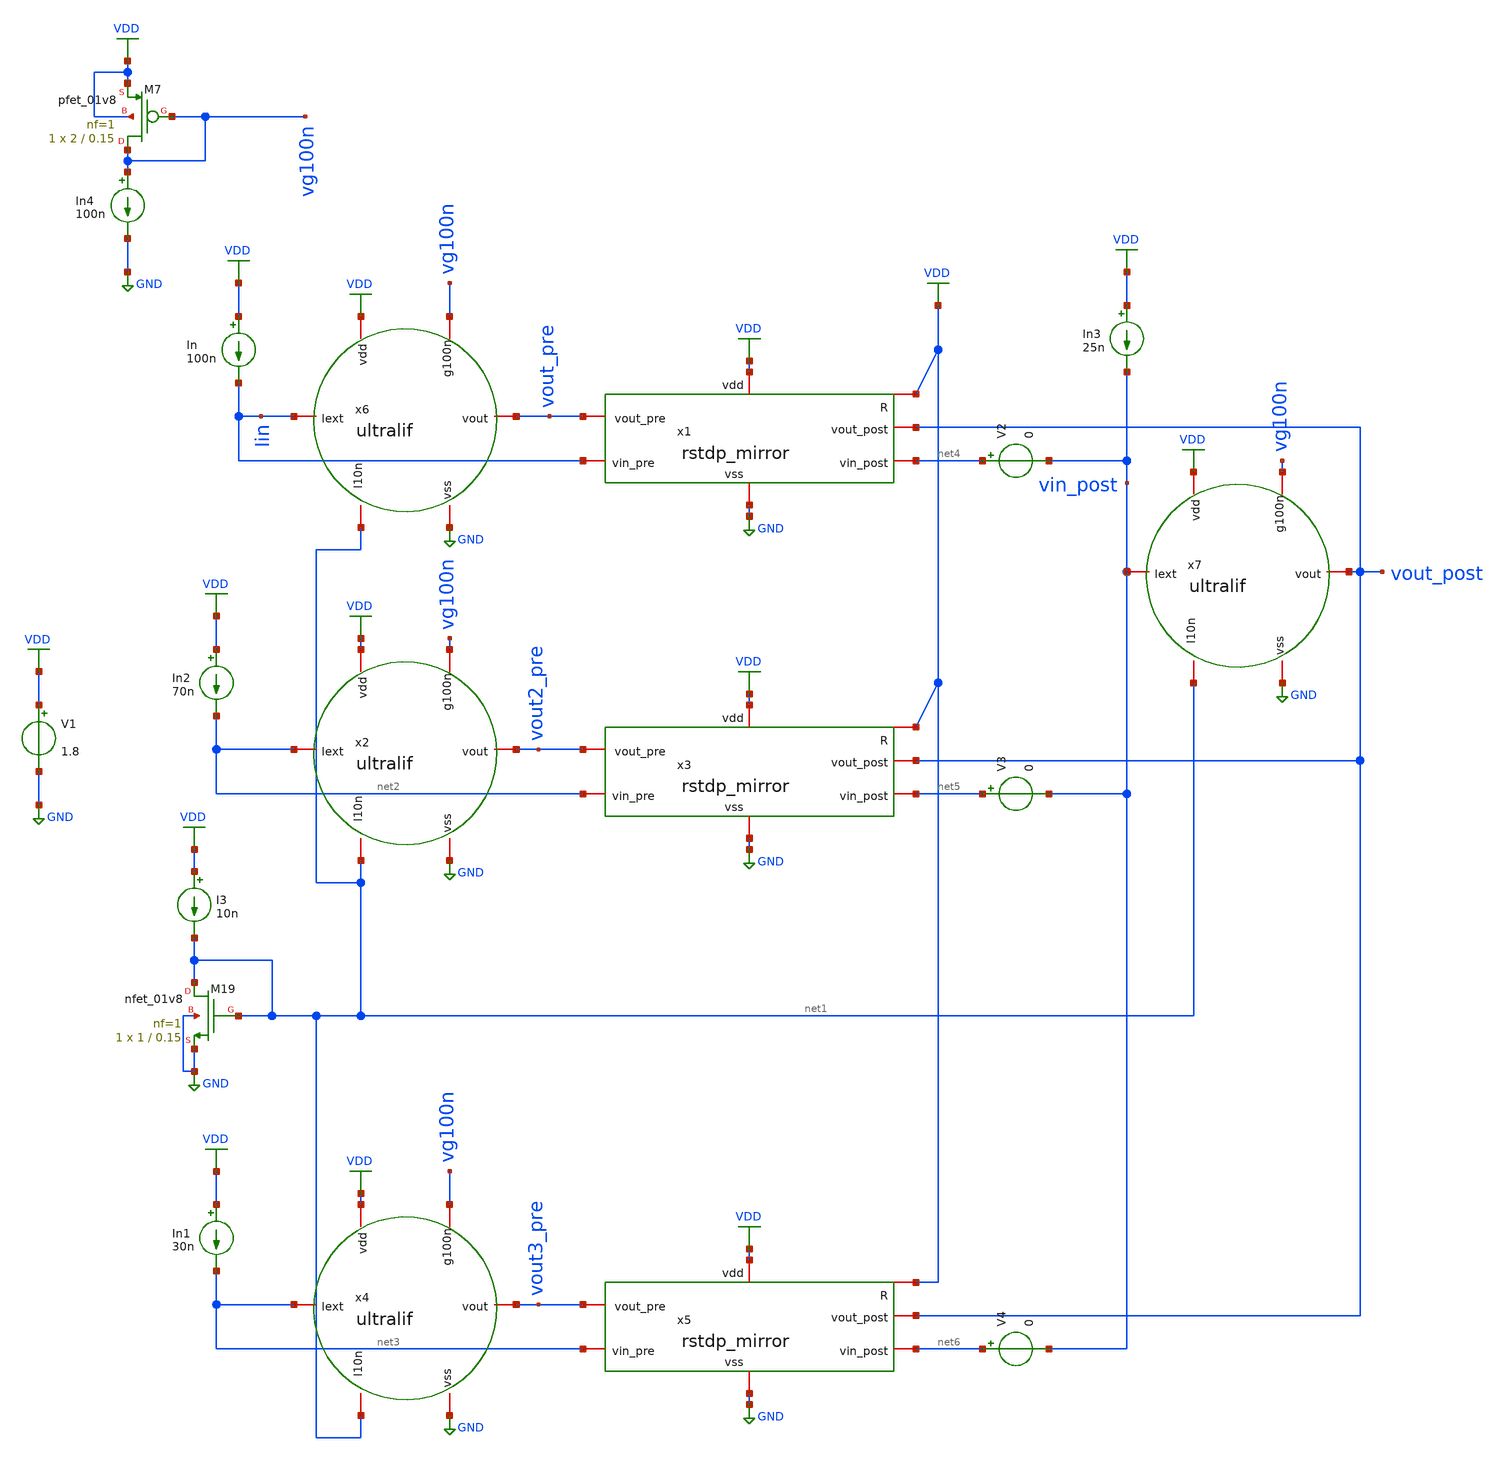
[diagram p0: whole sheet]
** sch_path: tb_3_1_mirror.sch
**.subckt tb_3_1_mirror
V1 VDD GND 1.8
x6 VDD Iin vout_pre net1 GND vg100n ultralif
x7 VDD vin_post vout_post net1 GND vg100n ultralif
XM19 net1 net1 GND GND sky130_fd_pr__nfet_01v8 L=0.15 W=1 nf=1 ad='int((nf+1)/2) * W/nf * 0.29' as='int((nf+2)/2) * W/nf * 0.29'
+ pd='2*int((nf+1)/2) * (W/nf + 0.29)' ps='2*int((nf+2)/2) * (W/nf + 0.29)' nrd='0.29 / W' nrs='0.29 / W'
+ sa=0 sb=0 sd=0 mult=1 m=1
I3 VDD net1 10n
In VDD Iin 100n
x2 VDD net2 vout2_pre net1 GND vg100n ultralif
In2 VDD net2 70n
x4 VDD net3 vout3_pre net1 GND vg100n ultralif
In1 VDD net3 30n
In3 VDD vin_post 25n
XM7 vg100n vg100n VDD VDD sky130_fd_pr__pfet_01v8 L=0.15 W=2 nf=1 ad='int((nf+1)/2) * W/nf * 0.29' as='int((nf+2)/2) * W/nf * 0.29'
+ pd='2*int((nf+1)/2) * (W/nf + 0.29)' ps='2*int((nf+2)/2) * (W/nf + 0.29)' nrd='0.29 / W' nrs='0.29 / W'
+ sa=0 sb=0 sd=0 mult=1 m=1
In4 vg100n GND 100n
x1 VDD VDD GND vout_pre vout_post net4 Iin rstdp_mirror
x3 VDD VDD GND vout2_pre vout_post net5 net2 rstdp_mirror
x5 VDD VDD GND vout3_pre vout_post net6 net3 rstdp_mirror
V2 net4 vin_post 0
V3 net5 vin_post 0
V4 net6 vin_post 0
**** begin user architecture code
.lib $::SKYWATER_MODELS/sky130.lib.spice tt

** opencircuitdesign pdks install
.inc $::SKYWATER_MODELS/rram_v0.spice

**** end user architecture code
**.ends

* expanding   symbol:  /home/alex/Desktop/EDA/SNN_IPN/Neuron/ultralif/ultralif.sym # of pins=6
** sym_path: Neuron/ultralif/ultralif.sym
** sch_path: Neuron/ultralif/ultralif.sch
.subckt ultralif vdd Iext vout I10n vss g100n
*.iopin Iext
*.iopin vout
*.iopin vss
*.iopin I10n
*.iopin vdd
*.iopin g100n
XM1 net2 net2 vm vdd sky130_fd_pr__pfet_01v8 L=10 W=1 nf=1 ad='int((nf+1)/2) * W/nf * 0.29' as='int((nf+2)/2) * W/nf * 0.29'
+ pd='2*int((nf+1)/2) * (W/nf + 0.29)' ps='2*int((nf+2)/2) * (W/nf + 0.29)' nrd='0.29 / W' nrs='0.29 / W'
+ sa=0 sb=0 sd=0 mult=1 m=1
XM2 net2 net1 vm vdd sky130_fd_pr__pfet_01v8 L=0.15 W=1.5 nf=1 ad='int((nf+1)/2) * W/nf * 0.29' as='int((nf+2)/2) * W/nf * 0.29'
+ pd='2*int((nf+1)/2) * (W/nf + 0.29)' ps='2*int((nf+2)/2) * (W/nf + 0.29)' nrd='0.29 / W' nrs='0.29 / W'
+ sa=0 sb=0 sd=0 mult=1 m=1
XM3 net1 net1 vm vdd sky130_fd_pr__pfet_01v8 L=0.15 W=5 nf=1 ad='int((nf+1)/2) * W/nf * 0.29' as='int((nf+2)/2) * W/nf * 0.29'
+ pd='2*int((nf+1)/2) * (W/nf + 0.29)' ps='2*int((nf+2)/2) * (W/nf + 0.29)' nrd='0.29 / W' nrs='0.29 / W'
+ sa=0 sb=0 sd=0 mult=2 m=2
XM4 net1 net2 vss vss sky130_fd_pr__nfet_01v8 L=4 W=1 nf=1 ad='int((1 + 1)/2) * 1 / 1 * 0.29' as='int((1 + 2)/2) * 1 / 1 * 0.29'
+ pd='2*int((1 + 1)/2) * (1 / 1 + 0.29)' ps='2*int((1 + 2)/2) * (1 / 1 + 0.29)' nrd='0.29 / 1 ' nrs='0.29 / 1 '
+ sa=0 sb=0 sd=0 mult=1 m=1
C1 vm vss 0.1p m=1
XM9 vm net2 Iext vdd sky130_fd_pr__pfet_01v8 L=0.15 W=2 nf=1 ad='int((nf+1)/2) * W/nf * 0.29' as='int((nf+2)/2) * W/nf * 0.29'
+ pd='2*int((nf+1)/2) * (W/nf + 0.29)' ps='2*int((nf+2)/2) * (W/nf + 0.29)' nrd='0.29 / W' nrs='0.29 / W'
+ sa=0 sb=0 sd=0 mult=1 m=1
XM10 net2 I10n vss vss sky130_fd_pr__nfet_01v8 L=0.15 W=1 nf=1 ad='int((1 + 1)/2) * 1 / 1 * 0.29' as='int((1 + 2)/2) * 1 / 1 * 0.29'
+ pd='2*int((1 + 1)/2) * (1 / 1 + 0.29)' ps='2*int((1 + 2)/2) * (1 / 1 + 0.29)' nrd='0.29 / 1 ' nrs='0.29 / 1 '
+ sa=0 sb=0 sd=0 mult=1 m=1
XM5 vout net2 vss vss sky130_fd_pr__nfet_01v8 L=0.15 W=1 nf=1 ad='int((1 + 1)/2) * 1 / 1 * 0.29' as='int((1 + 2)/2) * 1 / 1 * 0.29'
+ pd='2*int((1 + 1)/2) * (1 / 1 + 0.29)' ps='2*int((1 + 2)/2) * (1 / 1 + 0.29)' nrd='0.29 / 1 ' nrs='0.29 / 1 '
+ sa=0 sb=0 sd=0 mult=1 m=1
XM6 vout g100n vdd vdd sky130_fd_pr__pfet_01v8 L=0.15 W=2 nf=1 ad='int((nf+1)/2) * W/nf * 0.29' as='int((nf+2)/2) * W/nf * 0.29'
+ pd='2*int((nf+1)/2) * (W/nf + 0.29)' ps='2*int((nf+2)/2) * (W/nf + 0.29)' nrd='0.29 / W' nrs='0.29 / W'
+ sa=0 sb=0 sd=0 mult=1 m=1
.ends


* expanding   symbol:  /home/alex/Desktop/EDA/SNN_IPN/Synapse/rstdp_mirror.sym # of pins=7
** sym_path: Synapse/rstdp_mirror.sym
** sch_path: Synapse/rstdp_mirror.sch
.subckt rstdp_mirror vdd R vss vout_pre vout_post vin_post vin_pre
*.iopin vdd
*.iopin vss
*.iopin R
*.iopin vout_post
*.iopin vout_pre
*.iopin vin_post
*.iopin vin_pre
XR2 net1 be rram_v0
XM2 vpre R be vss sky130_fd_pr__nfet_01v8 L=0.15 W=7.5 nf=1 ad='int((nf+1)/2) * W/nf * 0.29' as='int((nf+2)/2) * W/nf * 0.29'
+ pd='2*int((nf+1)/2) * (W/nf + 0.29)' ps='2*int((nf+2)/2) * (W/nf + 0.29)' nrd='0.29 / W' nrs='0.29 / W'
+ sa=0 sb=0 sd=0 mult=1 m=1
XM3 te R vpost vss sky130_fd_pr__nfet_01v8 L=0.15 W=7.5 nf=1 ad='int((nf+1)/2) * W/nf * 0.29' as='int((nf+2)/2) * W/nf * 0.29'
+ pd='2*int((nf+1)/2) * (W/nf + 0.29)' ps='2*int((nf+2)/2) * (W/nf + 0.29)' nrd='0.29 / W' nrs='0.29 / W'
+ sa=0 sb=0 sd=0 mult=1 m=1
XM1 te R vpre vdd sky130_fd_pr__pfet_01v8 L=0.15 W=15 nf=1 ad='int((nf+1)/2) * W/nf * 0.29' as='int((nf+2)/2) * W/nf * 0.29'
+ pd='2*int((nf+1)/2) * (W/nf + 0.29)' ps='2*int((nf+2)/2) * (W/nf + 0.29)' nrd='0.29 / W' nrs='0.29 / W'
+ sa=0 sb=0 sd=0 mult=2 m=2
XM4 vpost R be vdd sky130_fd_pr__pfet_01v8 L=0.15 W=15 nf=1 ad='int((nf+1)/2) * W/nf * 0.29' as='int((nf+2)/2) * W/nf * 0.29'
+ pd='2*int((nf+1)/2) * (W/nf + 0.29)' ps='2*int((nf+2)/2) * (W/nf + 0.29)' nrd='0.29 / W' nrs='0.29 / W'
+ sa=0 sb=0 sd=0 mult=2 m=2
XM7 vpost vout_post vss vss sky130_fd_pr__nfet_01v8 L=0.15 W=1 nf=1 ad='int((1 + 1)/2) * 1 / 1 * 0.29'
+ as='int((1 + 2)/2) * 1 / 1 * 0.29' pd='2*int((1 + 1)/2) * (1 / 1 + 0.29)' ps='2*int((1 + 2)/2) * (1 / 1 + 0.29)'
+ nrd='0.29 / 1 ' nrs='0.29 / 1 ' sa=0 sb=0 sd=0 mult=1 m=1
XM5 vpost vout_post vdd vdd sky130_fd_pr__pfet_01v8 L=0.15 W=2 nf=1 ad='int((nf+1)/2) * W/nf * 0.29'
+ as='int((nf+2)/2) * W/nf * 0.29' pd='2*int((nf+1)/2) * (W/nf + 0.29)' ps='2*int((nf+2)/2) * (W/nf + 0.29)'
+ nrd='0.29 / W' nrs='0.29 / W' sa=0 sb=0 sd=0 mult=1 m=1
XM6 vpre vout_pre vss vss sky130_fd_pr__nfet_01v8 L=0.15 W=1 nf=1 ad='int((1 + 1)/2) * 1 / 1 * 0.29'
+ as='int((1 + 2)/2) * 1 / 1 * 0.29' pd='2*int((1 + 1)/2) * (1 / 1 + 0.29)' ps='2*int((1 + 2)/2) * (1 / 1 + 0.29)'
+ nrd='0.29 / 1 ' nrs='0.29 / 1 ' sa=0 sb=0 sd=0 mult=1 m=1
XM8 vpre vout_pre vdd vdd sky130_fd_pr__pfet_01v8 L=0.15 W=2 nf=1 ad='int((nf+1)/2) * W/nf * 0.29' as='int((nf+2)/2) * W/nf * 0.29'
+ pd='2*int((nf+1)/2) * (W/nf + 0.29)' ps='2*int((nf+2)/2) * (W/nf + 0.29)' nrd='0.29 / W' nrs='0.29 / W'
+ sa=0 sb=0 sd=0 mult=1 m=1
XM9 te te net1 vdd sky130_fd_pr__pfet_01v8 L=0.15 W=2 nf=1 ad='int((nf+1)/2) * W/nf * 0.29' as='int((nf+2)/2) * W/nf * 0.29'
+ pd='2*int((nf+1)/2) * (W/nf + 0.29)' ps='2*int((nf+2)/2) * (W/nf + 0.29)' nrd='0.29 / W' nrs='0.29 / W'
+ sa=0 sb=0 sd=0 mult=1 m=1
XM10 net2 te vdd vdd sky130_fd_pr__pfet_01v8 L=0.15 W=2 nf=1 ad='int((nf+1)/2) * W/nf * 0.29' as='int((nf+2)/2) * W/nf * 0.29'
+ pd='2*int((nf+1)/2) * (W/nf + 0.29)' ps='2*int((nf+2)/2) * (W/nf + 0.29)' nrd='0.29 / W' nrs='0.29 / W'
+ sa=0 sb=0 sd=0 mult=1 m=1
XM12 net1 net1 te vdd sky130_fd_pr__pfet_01v8 L=0.15 W=2 nf=1 ad='int((nf+1)/2) * W/nf * 0.29' as='int((nf+2)/2) * W/nf * 0.29'
+ pd='2*int((nf+1)/2) * (W/nf + 0.29)' ps='2*int((nf+2)/2) * (W/nf + 0.29)' nrd='0.29 / W' nrs='0.29 / W'
+ sa=0 sb=0 sd=0 mult=1 m=1
XM13 net3 net1 vdd vdd sky130_fd_pr__pfet_01v8 L=0.15 W=2 nf=1 ad='int((nf+1)/2) * W/nf * 0.29' as='int((nf+2)/2) * W/nf * 0.29'
+ pd='2*int((nf+1)/2) * (W/nf + 0.29)' ps='2*int((nf+2)/2) * (W/nf + 0.29)' nrd='0.29 / W' nrs='0.29 / W'
+ sa=0 sb=0 sd=0 mult=1 m=1
XM15 net2 net2 vin_post vss sky130_fd_pr__nfet_01v8 L=0.15 W=1 nf=1 ad='int((nf+1)/2) * W/nf * 0.29'
+ as='int((nf+2)/2) * W/nf * 0.29' pd='2*int((nf+1)/2) * (W/nf + 0.29)' ps='2*int((nf+2)/2) * (W/nf + 0.29)'
+ nrd='0.29 / W' nrs='0.29 / W' sa=0 sb=0 sd=0 mult=1 m=1
XM16 net3 net3 vin_pre vss sky130_fd_pr__nfet_01v8 L=0.15 W=1 nf=1 ad='int((nf+1)/2) * W/nf * 0.29' as='int((nf+2)/2) * W/nf * 0.29'
+ pd='2*int((nf+1)/2) * (W/nf + 0.29)' ps='2*int((nf+2)/2) * (W/nf + 0.29)' nrd='0.29 / W' nrs='0.29 / W'
+ sa=0 sb=0 sd=0 mult=1 m=1
.ends

.GLOBAL VDD
.GLOBAL GND
**** begin user architecture code


*.options savecurrents
.tran 50n 200u uic
.control
	run
	write tb_3_1_mirror.raw
.endc


**** end user architecture code
.end
